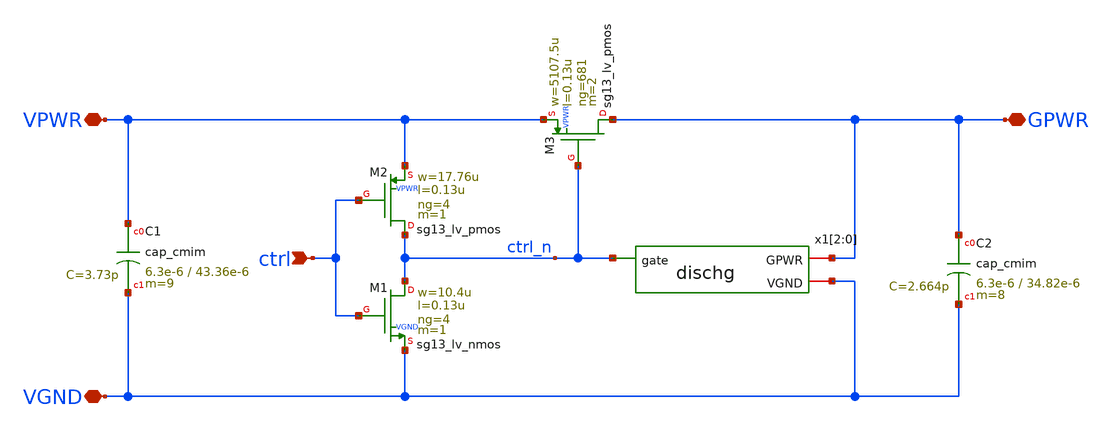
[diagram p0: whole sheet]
** sch_path: pg/ihp-sg13g2/tt_pg_1v5_hp_4/xschem/tt_pg_1v5_hp_4.sch
**.subckt tt_pg_1v5_hp_4 ctrl VPWR VGND GPWR
*.ipin ctrl
*.iopin VPWR
*.iopin VGND
*.iopin GPWR
XM1 ctrl_n ctrl VGND VGND sg13_lv_nmos w=10.4u l=0.13u ng=4 m=1
XM2 ctrl_n ctrl VPWR VPWR sg13_lv_pmos w=17.76u l=0.13u ng=4 m=1
XM3 GPWR ctrl_n VPWR VPWR sg13_lv_pmos w=5107.5u l=0.13u ng=681 m=2
XC1 VPWR VGND cap_cmim w=6.3e-6 l=43.36e-6 m=9 mm_ok=1
XC2 GPWR VGND cap_cmim w=6.3e-6 l=34.82e-6 m=8 mm_ok=1
x1[2] VGND GPWR ctrl_n dischg
x1[1] VGND GPWR ctrl_n dischg
x1[0] VGND GPWR ctrl_n dischg
**.ends

* expanding   symbol:  dischg.sym # of pins=3
** sym_path: pg/ihp-sg13g2/common/xschem/dischg.sym
** sch_path: pg/ihp-sg13g2/common/xschem/dischg.sch
.subckt dischg VGND GPWR gate
*.iopin GPWR
*.iopin VGND
*.ipin gate
XM1 GPWR gate net3 VGND sg13_lv_nmos w=0.50u l=0.65u ng=1 m=1
XM2 net3 gate net2 VGND sg13_lv_nmos w=0.50u l=0.65u ng=1 m=1
XM3 net2 gate net1 VGND sg13_lv_nmos w=0.50u l=0.65u ng=1 m=1
XM4 net1 gate VGND VGND sg13_lv_nmos w=0.50u l=0.65u ng=1 m=1
XM5 GPWR gate net6 VGND sg13_lv_nmos w=0.50u l=0.65u ng=1 m=1
XM6 net6 gate net5 VGND sg13_lv_nmos w=0.50u l=0.65u ng=1 m=1
XM7 net5 gate net4 VGND sg13_lv_nmos w=0.50u l=0.65u ng=1 m=1
XM8 net4 gate VGND VGND sg13_lv_nmos w=0.50u l=0.65u ng=1 m=1
.ends

.end
